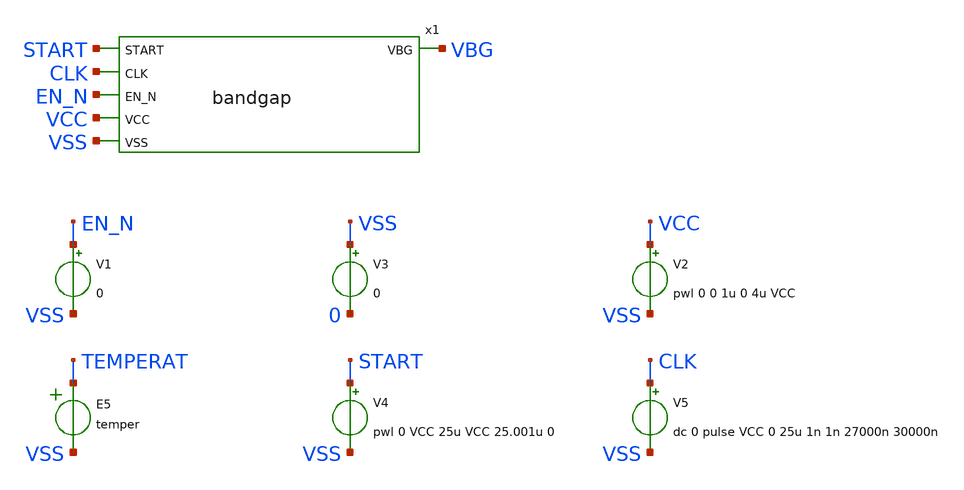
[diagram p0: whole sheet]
** sch_path: sky130_tests/tb_bandgap.sch
* Copyright 2021 Stefan Frederik Schippers
* Licensed under the Apache License, Version 2.0 (the "License");
* you may not use this file except in compliance with the License.
* You may obtain a copy of the License at
* https://www.apache.org/licenses/LICENSE-2.0
* Unless required by applicable law or agreed to in writing, software
* distributed under the License is distributed on an "AS IS" BASIS,
* WITHOUT WARRANTIES OR CONDITIONS OF ANY KIND, either express or implied.
* See the License for the specific language governing permissions and
* limitations under the License.
**.subckt tb_bandgap
x1 START CLK EN_N VBG VCC VSS bandgap
V1 EN_N VSS 0
V2 VCC VSS pwl 0 0 1u 0 4u VCC
V3 VSS 0 0
E5 TEMPERAT VSS VOL=' temper '
V4 START VSS pwl 0 VCC 25u VCC 25.001u 0
V5 CLK VSS dc 0 pulse VCC 0 25u 1n 1n 27000n 30000n
**** begin user architecture code


* this experimental option enables mos model bin
* selection based on W/NF instead of W
.options wnflag=1 XMU=0.49 METHOD=GEAR ITL4=100 CHGTOL=1e-15 TRTOL=1 RELTOL=0.0001 VNTOL=0.1u
.param ABSVAR=0.03
.param VCCGAUSS=agauss(1.8, 'ABSVAR', 1)
.param VCC=VCCGAUSS
* .param VCC=1.8
** variation marameters:
* .options savecurrents
.control
  option seed=12
  let run=1
  dowhile run <= 14
    if run > 1
      reset
      set appendwrite
    end
    * save vbg x1.plus x1.minus i(v2) vcc
    save all
    if run % 3 = 0
      set temp=-40
    end
    if run % 3 = 1
      set temp=27
    end
    if run % 3 = 2
      set temp=125
    end
    tran 0.05u 150u
    write tb_bandgap.raw
    let run = run + 1
  end
  set nolegend
  plot all.vbg
.endc


 ** manual skywater pdks install (with patches applied)
* .lib $::SKYWATER_MODELS/models/sky130.lib.spice tt_mm

** opencircuitdesign pdks install
.lib $::SKYWATER_MODELS/sky130.lib.spice tt_mm


**** end user architecture code
**.ends
.end
